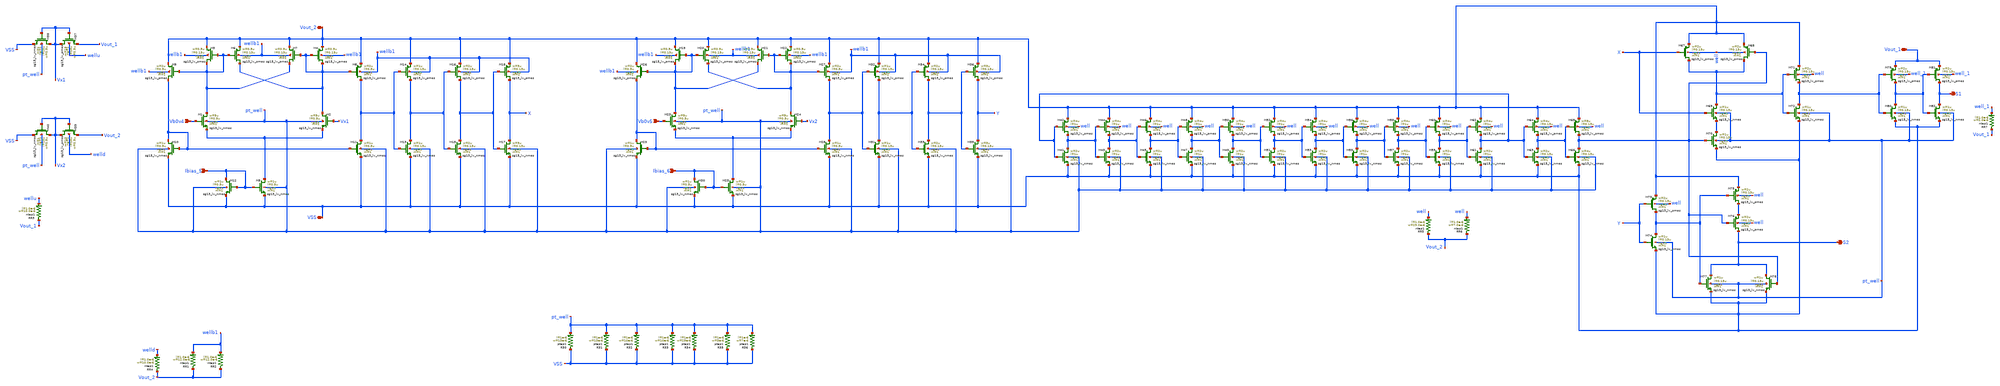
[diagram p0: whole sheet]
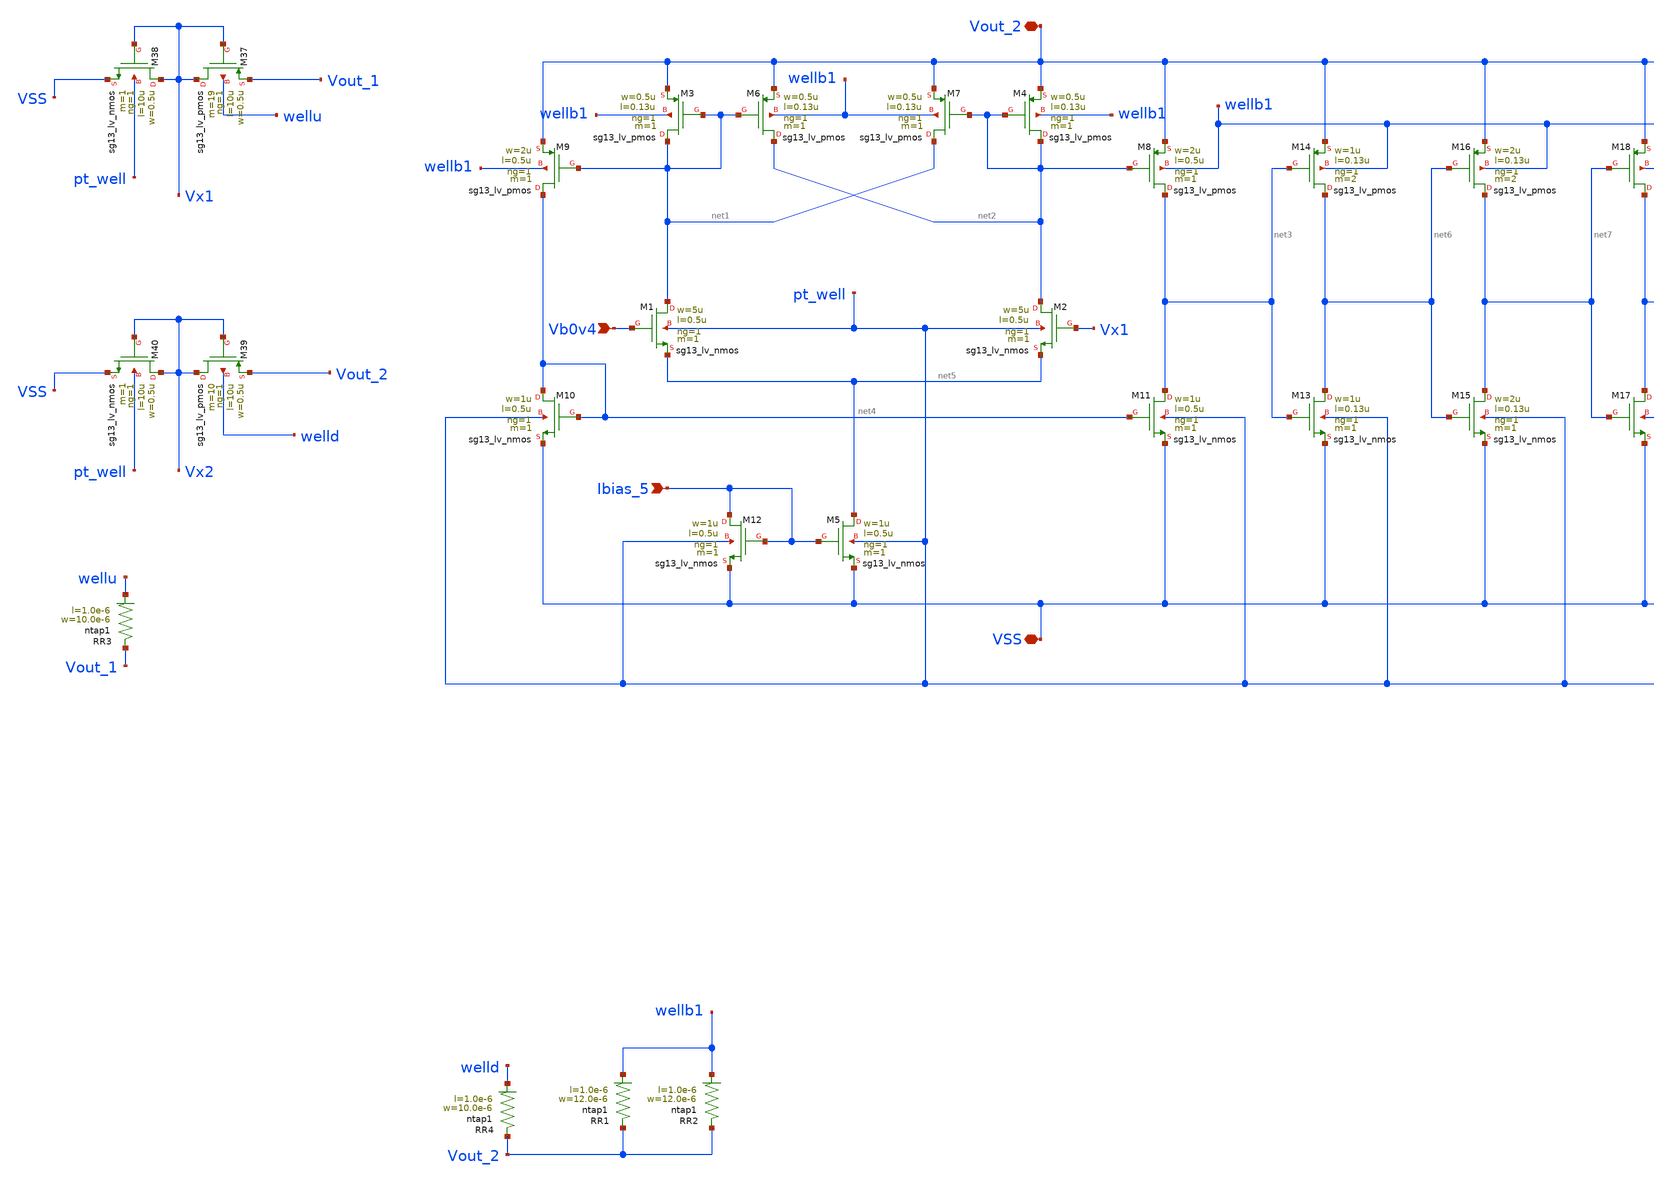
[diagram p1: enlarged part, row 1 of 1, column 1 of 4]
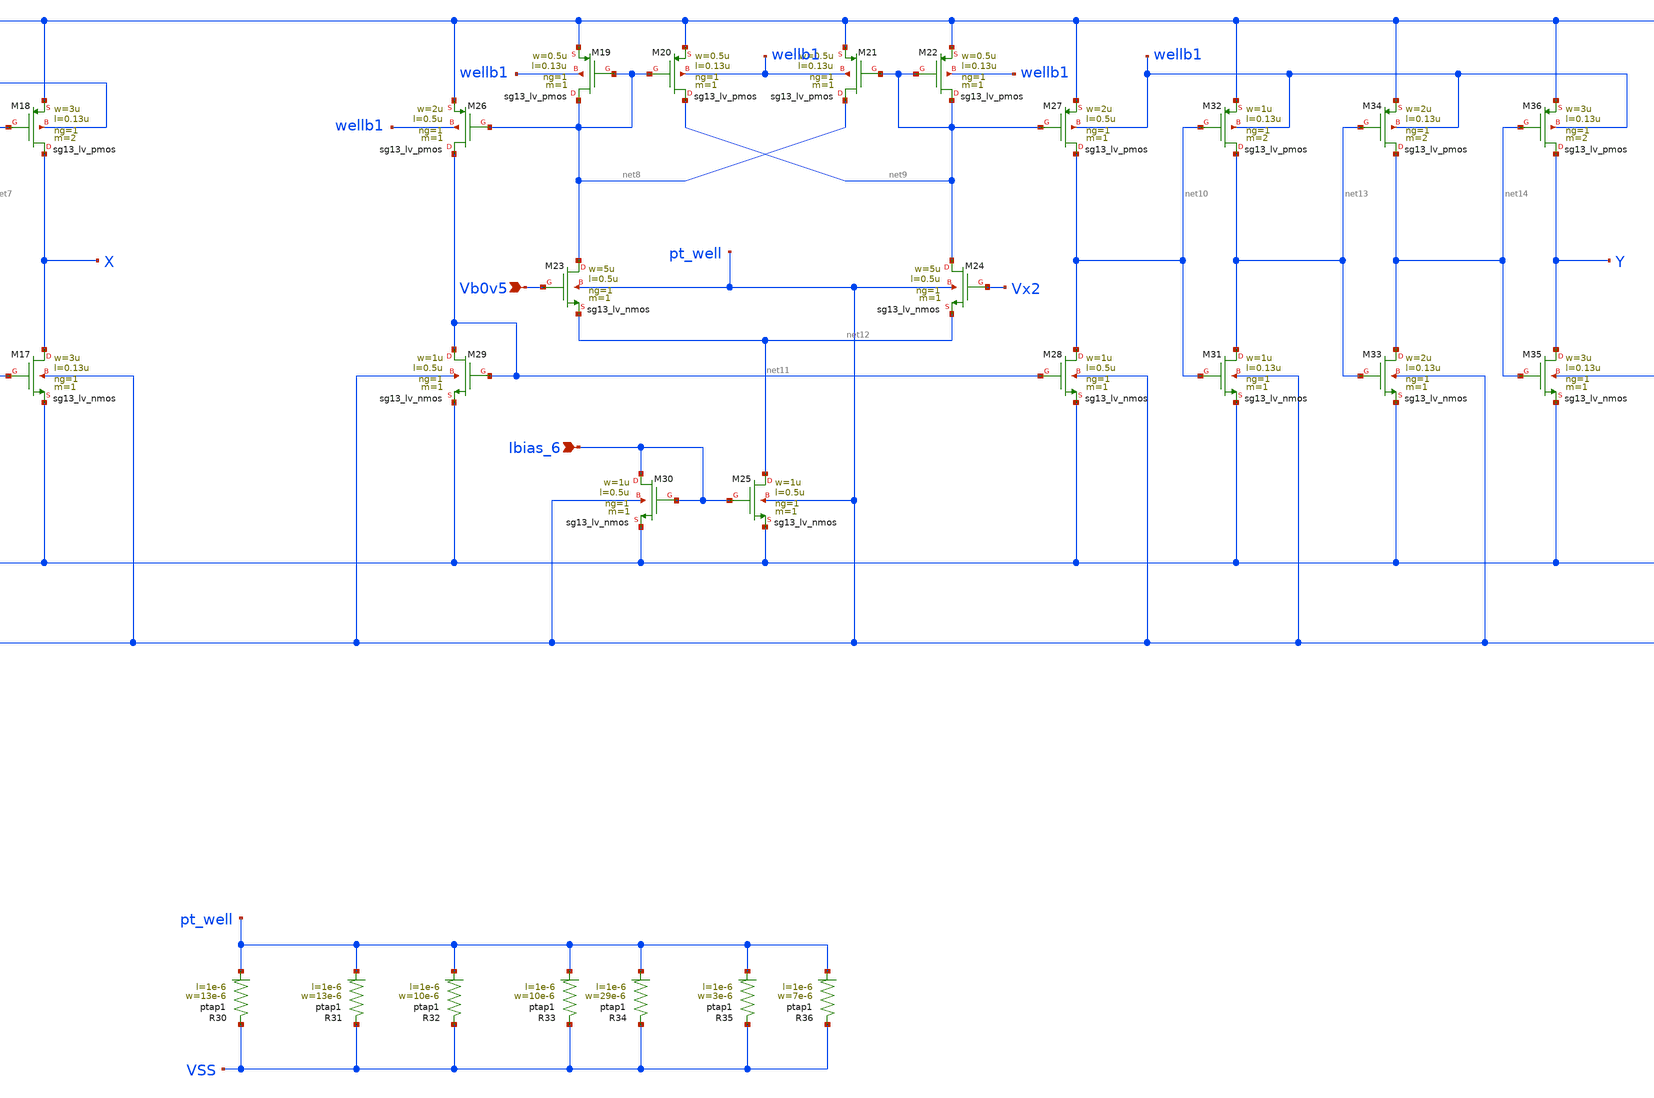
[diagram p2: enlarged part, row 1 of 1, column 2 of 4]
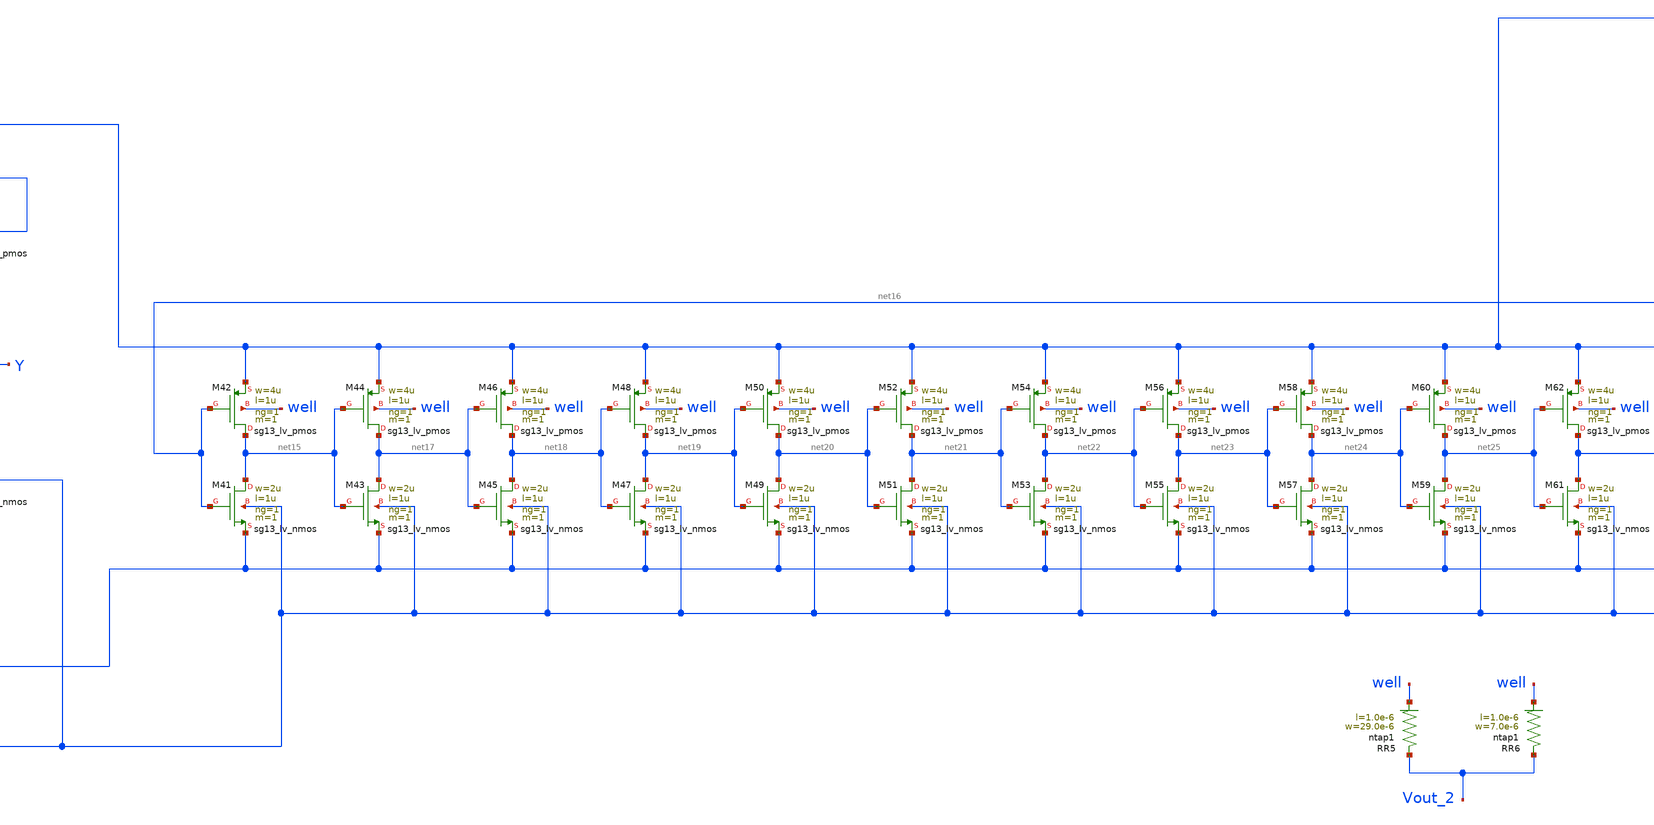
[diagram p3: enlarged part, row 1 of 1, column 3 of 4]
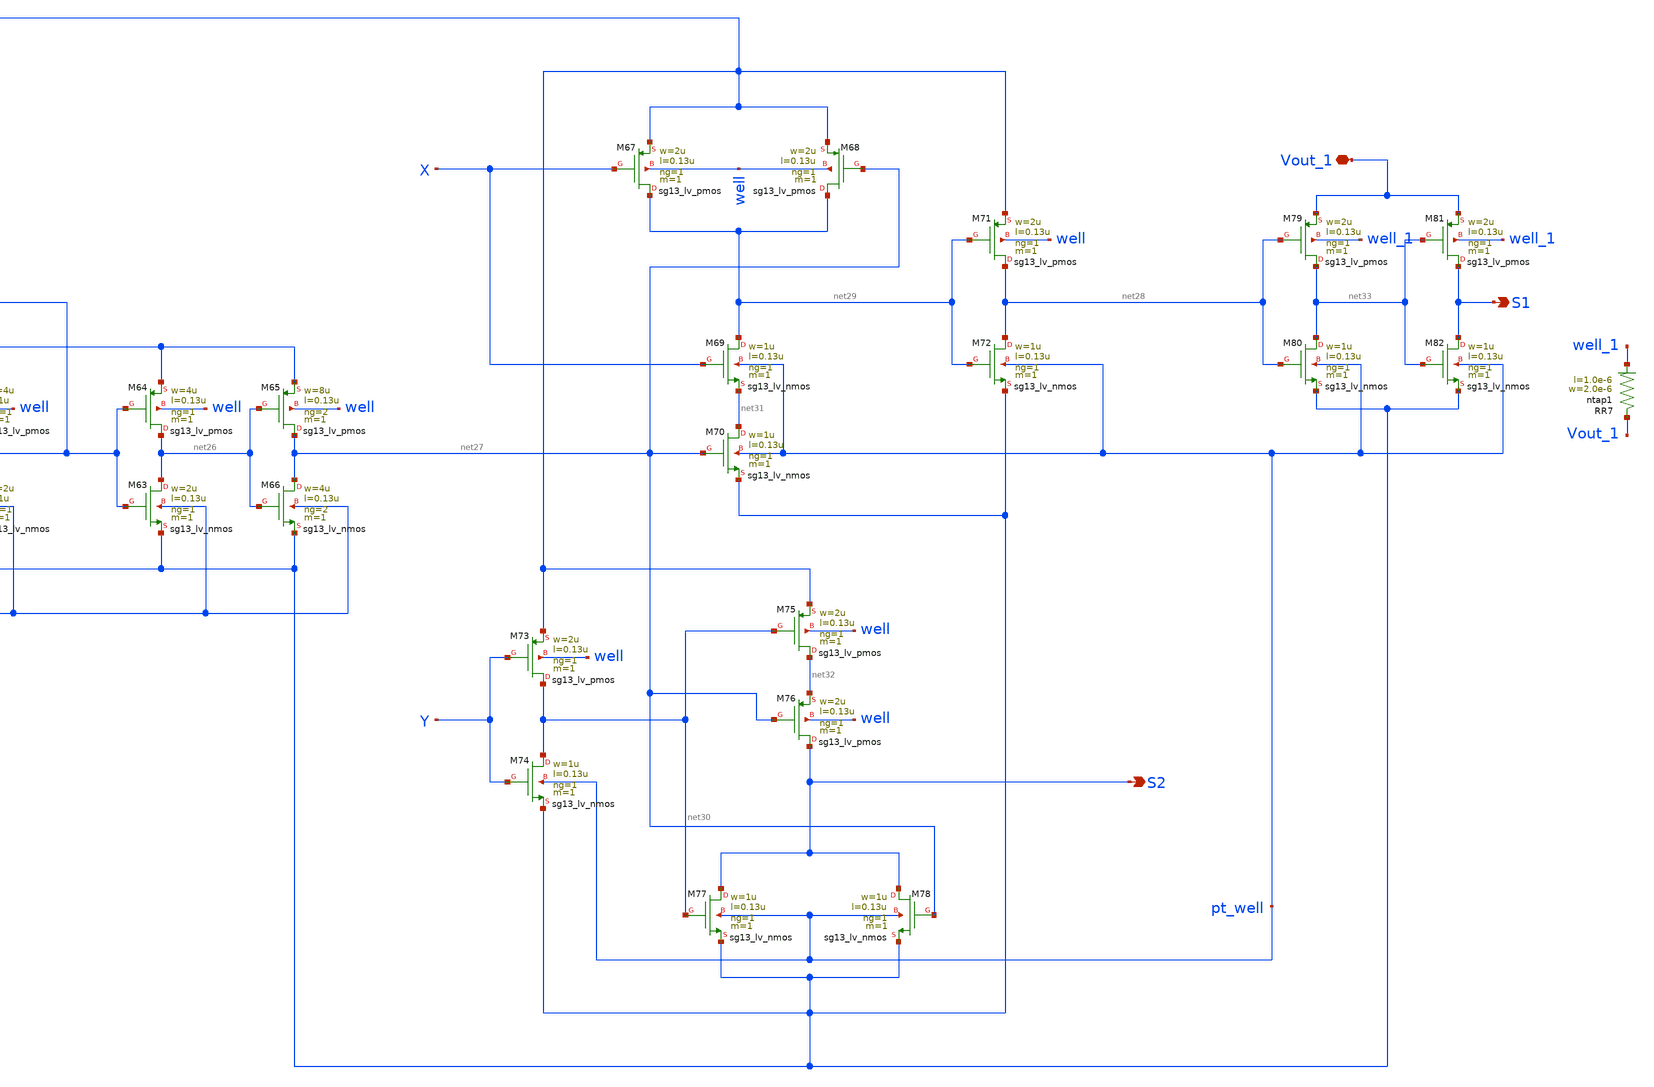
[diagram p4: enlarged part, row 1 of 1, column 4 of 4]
** sch_path: Layouts/Dig_control/dig_control.sch
**.subckt dig_control Vb0v4 VSS Vout_2 Vb0v5 Ibias_5 Ibias_6 S2 S1 Vout_1
*.ipin Vb0v4
*.iopin VSS
*.iopin Vout_2
*.ipin Vb0v5
*.ipin Ibias_5
*.ipin Ibias_6
*.opin S2
*.opin S1
*.iopin Vout_1
XM3 net1 net1 Vout_2 wellb1 sg13_lv_pmos w=0.5u l=0.13u ng=1 m=1 mm_ok=1
XM6 net2 net1 Vout_2 wellb1 sg13_lv_pmos w=0.5u l=0.13u ng=1 m=1 mm_ok=1
XM7 net1 net2 Vout_2 wellb1 sg13_lv_pmos w=0.5u l=0.13u ng=1 m=1 mm_ok=1
XM4 net2 net2 Vout_2 wellb1 sg13_lv_pmos w=0.5u l=0.13u ng=1 m=1 mm_ok=1
XM1 net1 Vb0v4 net5 pt_well sg13_lv_nmos w=5u l=0.5u ng=1 m=1 mm_ok=1
XM2 net2 Vx1 net5 pt_well sg13_lv_nmos w=5u l=0.5u ng=1 m=1 mm_ok=1
XM5 net5 Ibias_5 VSS pt_well sg13_lv_nmos w=1u l=0.5u ng=1 m=1 mm_ok=1
XM9 net4 net1 Vout_2 wellb1 sg13_lv_pmos w=2u l=0.5u ng=1 m=1 mm_ok=1
XM8 net3 net2 Vout_2 wellb1 sg13_lv_pmos w=2u l=0.5u ng=1 m=1 mm_ok=1
XM11 net3 net4 VSS pt_well sg13_lv_nmos w=1u l=0.5u ng=1 m=1 mm_ok=1
XM10 net4 net4 VSS pt_well sg13_lv_nmos w=1u l=0.5u ng=1 m=1 mm_ok=1
XM12 Ibias_5 Ibias_5 VSS pt_well sg13_lv_nmos w=1u l=0.5u ng=1 m=1 mm_ok=1
XM13 net6 net3 VSS pt_well sg13_lv_nmos w=1u l=0.13u ng=1 m=1 mm_ok=1
XM14 net6 net3 Vout_2 wellb1 sg13_lv_pmos w=1u l=0.13u ng=1 m=2 mm_ok=1
XM15 net7 net6 VSS pt_well sg13_lv_nmos w=2u l=0.13u ng=1 m=1 mm_ok=1
XM16 net7 net6 Vout_2 wellb1 sg13_lv_pmos w=2u l=0.13u ng=1 m=2 mm_ok=1
XM17 X net7 VSS pt_well sg13_lv_nmos w=3u l=0.13u ng=1 m=1 mm_ok=1
XM18 X net7 Vout_2 wellb1 sg13_lv_pmos w=3u l=0.13u ng=1 m=2 mm_ok=1
XM19 net8 net8 Vout_2 wellb1 sg13_lv_pmos w=0.5u l=0.13u ng=1 m=1 mm_ok=1
XM20 net9 net8 Vout_2 wellb1 sg13_lv_pmos w=0.5u l=0.13u ng=1 m=1 mm_ok=1
XM21 net8 net9 Vout_2 wellb1 sg13_lv_pmos w=0.5u l=0.13u ng=1 m=1 mm_ok=1
XM22 net9 net9 Vout_2 wellb1 sg13_lv_pmos w=0.5u l=0.13u ng=1 m=1 mm_ok=1
XM23 net8 Vb0v5 net12 pt_well sg13_lv_nmos w=5u l=0.5u ng=1 m=1 mm_ok=1
XM24 net9 Vx2 net12 pt_well sg13_lv_nmos w=5u l=0.5u ng=1 m=1 mm_ok=1
XM25 net12 Ibias_6 VSS pt_well sg13_lv_nmos w=1u l=0.5u ng=1 m=1 mm_ok=1
XM26 net11 net8 Vout_2 wellb1 sg13_lv_pmos w=2u l=0.5u ng=1 m=1 mm_ok=1
XM27 net10 net9 Vout_2 wellb1 sg13_lv_pmos w=2u l=0.5u ng=1 m=1 mm_ok=1
XM28 net10 net11 VSS pt_well sg13_lv_nmos w=1u l=0.5u ng=1 m=1 mm_ok=1
XM29 net11 net11 VSS pt_well sg13_lv_nmos w=1u l=0.5u ng=1 m=1 mm_ok=1
XM30 Ibias_6 Ibias_6 VSS pt_well sg13_lv_nmos w=1u l=0.5u ng=1 m=1 mm_ok=1
XM31 net13 net10 VSS pt_well sg13_lv_nmos w=1u l=0.13u ng=1 m=1 mm_ok=1
XM32 net13 net10 Vout_2 wellb1 sg13_lv_pmos w=1u l=0.13u ng=1 m=2 mm_ok=1
XM33 net14 net13 VSS pt_well sg13_lv_nmos w=2u l=0.13u ng=1 m=1 mm_ok=1
XM34 net14 net13 Vout_2 wellb1 sg13_lv_pmos w=2u l=0.13u ng=1 m=2 mm_ok=1
XM35 Y net14 VSS pt_well sg13_lv_nmos w=3u l=0.13u ng=1 m=1 mm_ok=1
XM36 Y net14 Vout_2 wellb1 sg13_lv_pmos w=3u l=0.13u ng=1 m=2 mm_ok=1
XM37 Vx1 Vx1 Vout_1 wellu sg13_lv_pmos w=0.5u l=10u ng=1 m=19 mm_ok=1
XM38 Vx1 Vx1 VSS pt_well sg13_lv_nmos w=0.5u l=10u ng=1 m=1 mm_ok=1
XM39 Vx2 Vx2 Vout_2 welld sg13_lv_pmos w=0.5u l=10u ng=1 m=10 mm_ok=1
XM40 Vx2 Vx2 VSS pt_well sg13_lv_nmos w=0.5u l=10u ng=1 m=1 mm_ok=1
XR1 Vout_2 wellb1 ntap1 R=25.79 w=12.0e-6 l=1.0e-6
XR2 Vout_2 wellb1 ntap1 R=25.79 w=12.0e-6 l=1.0e-6
XR3 Vout_1 wellu ntap1 R=30.62 w=10.0e-6 l=1.0e-6
XR4 Vout_2 welld ntap1 R=30.62 w=10.0e-6 l=1.0e-6
XM41 net15 net16 VSS pt_well sg13_lv_nmos w=2u l=1u ng=1 m=1 mm_ok=1
XM42 net15 net16 Vout_2 well sg13_lv_pmos w=4u l=1u ng=1 m=1 mm_ok=1
XM43 net17 net15 VSS pt_well sg13_lv_nmos w=2u l=1u ng=1 m=1 mm_ok=1
XM44 net17 net15 Vout_2 well sg13_lv_pmos w=4u l=1u ng=1 m=1 mm_ok=1
XM45 net18 net17 VSS pt_well sg13_lv_nmos w=2u l=1u ng=1 m=1 mm_ok=1
XM46 net18 net17 Vout_2 well sg13_lv_pmos w=4u l=1u ng=1 m=1 mm_ok=1
XM47 net19 net18 VSS pt_well sg13_lv_nmos w=2u l=1u ng=1 m=1 mm_ok=1
XM48 net19 net18 Vout_2 well sg13_lv_pmos w=4u l=1u ng=1 m=1 mm_ok=1
XM49 net20 net19 VSS pt_well sg13_lv_nmos w=2u l=1u ng=1 m=1 mm_ok=1
XM50 net20 net19 Vout_2 well sg13_lv_pmos w=4u l=1u ng=1 m=1 mm_ok=1
XM51 net21 net20 VSS pt_well sg13_lv_nmos w=2u l=1u ng=1 m=1 mm_ok=1
XM52 net21 net20 Vout_2 well sg13_lv_pmos w=4u l=1u ng=1 m=1 mm_ok=1
XM53 net22 net21 VSS pt_well sg13_lv_nmos w=2u l=1u ng=1 m=1 mm_ok=1
XM54 net22 net21 Vout_2 well sg13_lv_pmos w=4u l=1u ng=1 m=1 mm_ok=1
XM55 net23 net22 VSS pt_well sg13_lv_nmos w=2u l=1u ng=1 m=1 mm_ok=1
XM56 net23 net22 Vout_2 well sg13_lv_pmos w=4u l=1u ng=1 m=1 mm_ok=1
XM57 net24 net23 VSS pt_well sg13_lv_nmos w=2u l=1u ng=1 m=1 mm_ok=1
XM58 net24 net23 Vout_2 well sg13_lv_pmos w=4u l=1u ng=1 m=1 mm_ok=1
XM59 net25 net24 VSS pt_well sg13_lv_nmos w=2u l=1u ng=1 m=1 mm_ok=1
XM60 net25 net24 Vout_2 well sg13_lv_pmos w=4u l=1u ng=1 m=1 mm_ok=1
XM61 net16 net25 VSS pt_well sg13_lv_nmos w=2u l=1u ng=1 m=1 mm_ok=1
XM62 net16 net25 Vout_2 well sg13_lv_pmos w=4u l=1u ng=1 m=1 mm_ok=1
XM63 net26 net16 VSS pt_well sg13_lv_nmos w=2u l=0.13u ng=1 m=1 mm_ok=1
XM64 net26 net16 Vout_2 well sg13_lv_pmos w=4u l=0.13u ng=1 m=1 mm_ok=1
XM65 net27 net26 Vout_2 well sg13_lv_pmos w=8u l=0.13u ng=2 m=1 mm_ok=1
XM66 net27 net26 VSS pt_well sg13_lv_nmos w=4u l=0.13u ng=2 m=1 mm_ok=1
XR5 Vout_2 well ntap1 R=11.01 w=29.0e-6 l=1.0e-6
XM67 net29 X Vout_2 well sg13_lv_pmos w=2u l=0.13u ng=1 m=1 mm_ok=1
XM68 net29 net27 Vout_2 well sg13_lv_pmos w=2u l=0.13u ng=1 m=1 mm_ok=1
XM69 net29 X net31 pt_well sg13_lv_nmos w=1u l=0.13u ng=1 m=1 mm_ok=1
XM70 net31 net27 VSS pt_well sg13_lv_nmos w=1u l=0.13u ng=1 m=1 mm_ok=1
XM71 net28 net29 Vout_2 well sg13_lv_pmos w=2u l=0.13u ng=1 m=1 mm_ok=1
XM72 net28 net29 VSS pt_well sg13_lv_nmos w=1u l=0.13u ng=1 m=1 mm_ok=1
XM73 net30 Y Vout_2 well sg13_lv_pmos w=2u l=0.13u ng=1 m=1 mm_ok=1
XM74 net30 Y VSS pt_well sg13_lv_nmos w=1u l=0.13u ng=1 m=1 mm_ok=1
XM75 net32 net30 Vout_2 well sg13_lv_pmos w=2u l=0.13u ng=1 m=1 mm_ok=1
XM76 S2 net27 net32 well sg13_lv_pmos w=2u l=0.13u ng=1 m=1 mm_ok=1
XM77 S2 net30 VSS pt_well sg13_lv_nmos w=1u l=0.13u ng=1 m=1 mm_ok=1
XM78 S2 net27 VSS pt_well sg13_lv_nmos w=1u l=0.13u ng=1 m=1 mm_ok=1
XR6 Vout_2 well ntap1 R=42.61 w=7.0e-6 l=1.0e-6
XM79 net33 net28 Vout_1 well_1 sg13_lv_pmos w=2u l=0.13u ng=1 m=1 mm_ok=1
XM80 net33 net28 VSS pt_well sg13_lv_nmos w=1u l=0.13u ng=1 m=1 mm_ok=1
XM81 S1 net33 Vout_1 well_1 sg13_lv_pmos w=2u l=0.13u ng=1 m=1 mm_ok=1
XM82 S1 net33 VSS pt_well sg13_lv_nmos w=1u l=0.13u ng=1 m=1 mm_ok=1
XR7 Vout_1 well_1 ntap1 R=122.5 w=2.0e-6 l=1.0e-6
XR30 VSS pt_well ptap1 R=23.9 w=13e-6 l=1e-6
XR32 VSS pt_well ptap1 R=30.62 w=10e-6 l=1e-6
XR34 VSS pt_well ptap1 R=11.01 w=29e-6 l=1e-6
XR35 VSS pt_well ptap1 R=89.09 w=3e-6 l=1e-6
XR36 VSS pt_well ptap1 R=42.61 w=7e-6 l=1e-6
XR31 VSS pt_well ptap1 R=23.9 w=13e-6 l=1e-6
XR33 VSS pt_well ptap1 R=30.62 w=10e-6 l=1e-6
**.ends
.end
